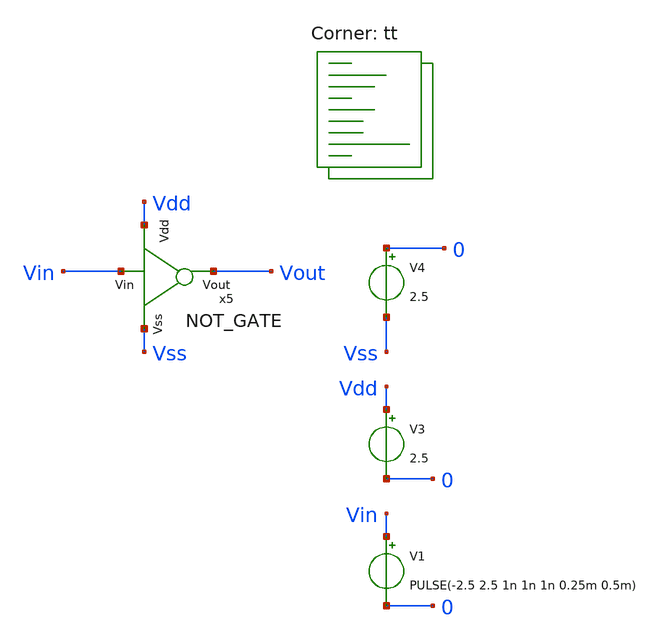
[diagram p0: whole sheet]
** sch_path: xschem/BASIC.sch
**.subckt BASIC
x5 Vdd Vout Vin Vss NOT_GATE
V4 0 Vss 2.5
V3 Vdd 0 2.5
V1 Vin 0 PULSE(-2.5 2.5 1n 1n 1n 0.25m 0.5m)
**** begin user architecture code
.lib $::SKYWATER_MODELS/sky130.lib.spice tt



**** end user architecture code
**.ends

* expanding   symbol:  NOT_GATE.sym # of pins=4
** sym_path: xschem/NOT_GATE.sym
** sch_path: xschem/NOT_GATE.sch
.subckt NOT_GATE Vdd Vout Vin Vss
*.opin Vout
*.ipin Vdd
*.ipin Vss
*.ipin Vin
XM1 Vout Vin Vss Vss sky130_fd_pr__nfet_g5v0d10v5 L=1 W=1 nf=1 ad='int((1 + 1)/2) * 1 / 1 * 0.29' as='int((1 + 2)/2) * 1 / 1 * 0.29'
+ pd='2*int((1 + 1)/2) * (1 / 1 + 0.29)' ps='2*int((1 + 2)/2) * (1 / 1 + 0.29)' nrd='0.29 / 1 ' nrs='0.29 / 1 '
+ sa=0 sb=0 sd=0 mult=1 m=1
XM2 Vout Vin Vdd Vdd sky130_fd_pr__pfet_g5v0d10v5 L=1 W=3 nf=1 ad='int((1 + 1)/2) * 3 / 1 * 0.29' as='int((1 + 2)/2) * 3 / 1 * 0.29'
+ pd='2*int((1 + 1)/2) * (3 / 1 + 0.29)' ps='2*int((1 + 2)/2) * (3 / 1 + 0.29)' nrd='0.29 / 3 ' nrs='0.29 / 3 '
+ sa=0 sb=0 sd=0 mult=1 m=1
.ends

.end
